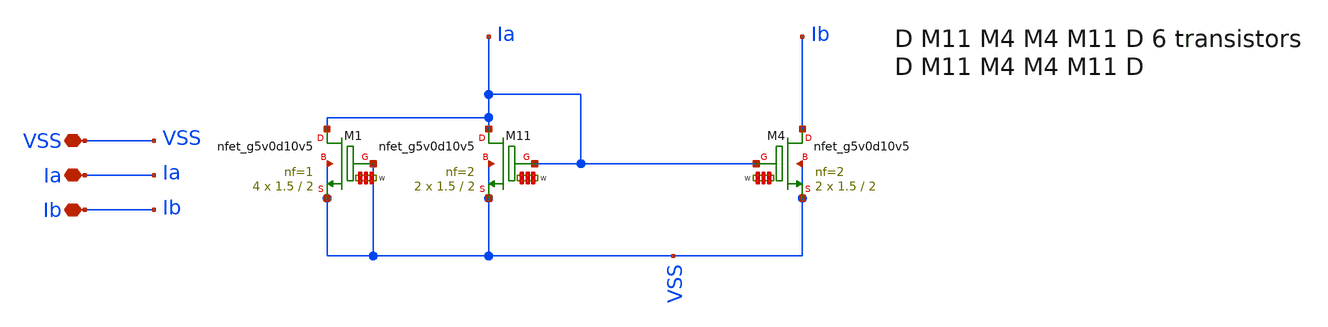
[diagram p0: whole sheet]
** sch_path: Learning/single_ended_amplifiers/Design_and_Analysis_of_Two-Stage_CMOS_Operational_Amplifier_for_Fluorescence_Signal_Processing_sky130_5V/layout_magic/active_load.sch
**.subckt active_load VSS Ia Ib
*.iopin VSS
*.iopin Ia
*.iopin Ib
XM4 Ib Ia VSS VSS sky130_fd_pr__nfet_g5v0d10v5 L=2 W='1.5 * 2 ' nf=2 ad='int((nf+1)/2) * W / nf * 0.29'
+ as='int((nf+2)/2) * W / nf * 0.29' pd='2*int((nf+1)/2) * (W / nf + 0.29)' ps='2*int((nf+2)/2) * (W / nf + 0.29)'
+ nrd='0.29 / W ' nrs='0.29 / W ' sa=0 sb=0 sd=0 mult=2 m=2
XM11 Ia Ia VSS VSS sky130_fd_pr__nfet_g5v0d10v5 L=2 W='1.5 * 2 ' nf=2 ad='int((nf+1)/2) * W / nf * 0.29'
+ as='int((nf+2)/2) * W / nf * 0.29' pd='2*int((nf+1)/2) * (W / nf + 0.29)' ps='2*int((nf+2)/2) * (W / nf + 0.29)'
+ nrd='0.29 / W ' nrs='0.29 / W ' sa=0 sb=0 sd=0 mult=2 m=2
XM1 Ia VSS VSS VSS sky130_fd_pr__nfet_g5v0d10v5 L=2 W='1.5 * 1 ' nf=1 ad='int((nf+1)/2) * W / nf * 0.29'
+ as='int((nf+2)/2) * W / nf * 0.29' pd='2*int((nf+1)/2) * (W / nf + 0.29)' ps='2*int((nf+2)/2) * (W / nf + 0.29)'
+ nrd='0.29 / W ' nrs='0.29 / W ' sa=0 sb=0 sd=0 mult=4 m=4
**.ends
.end
